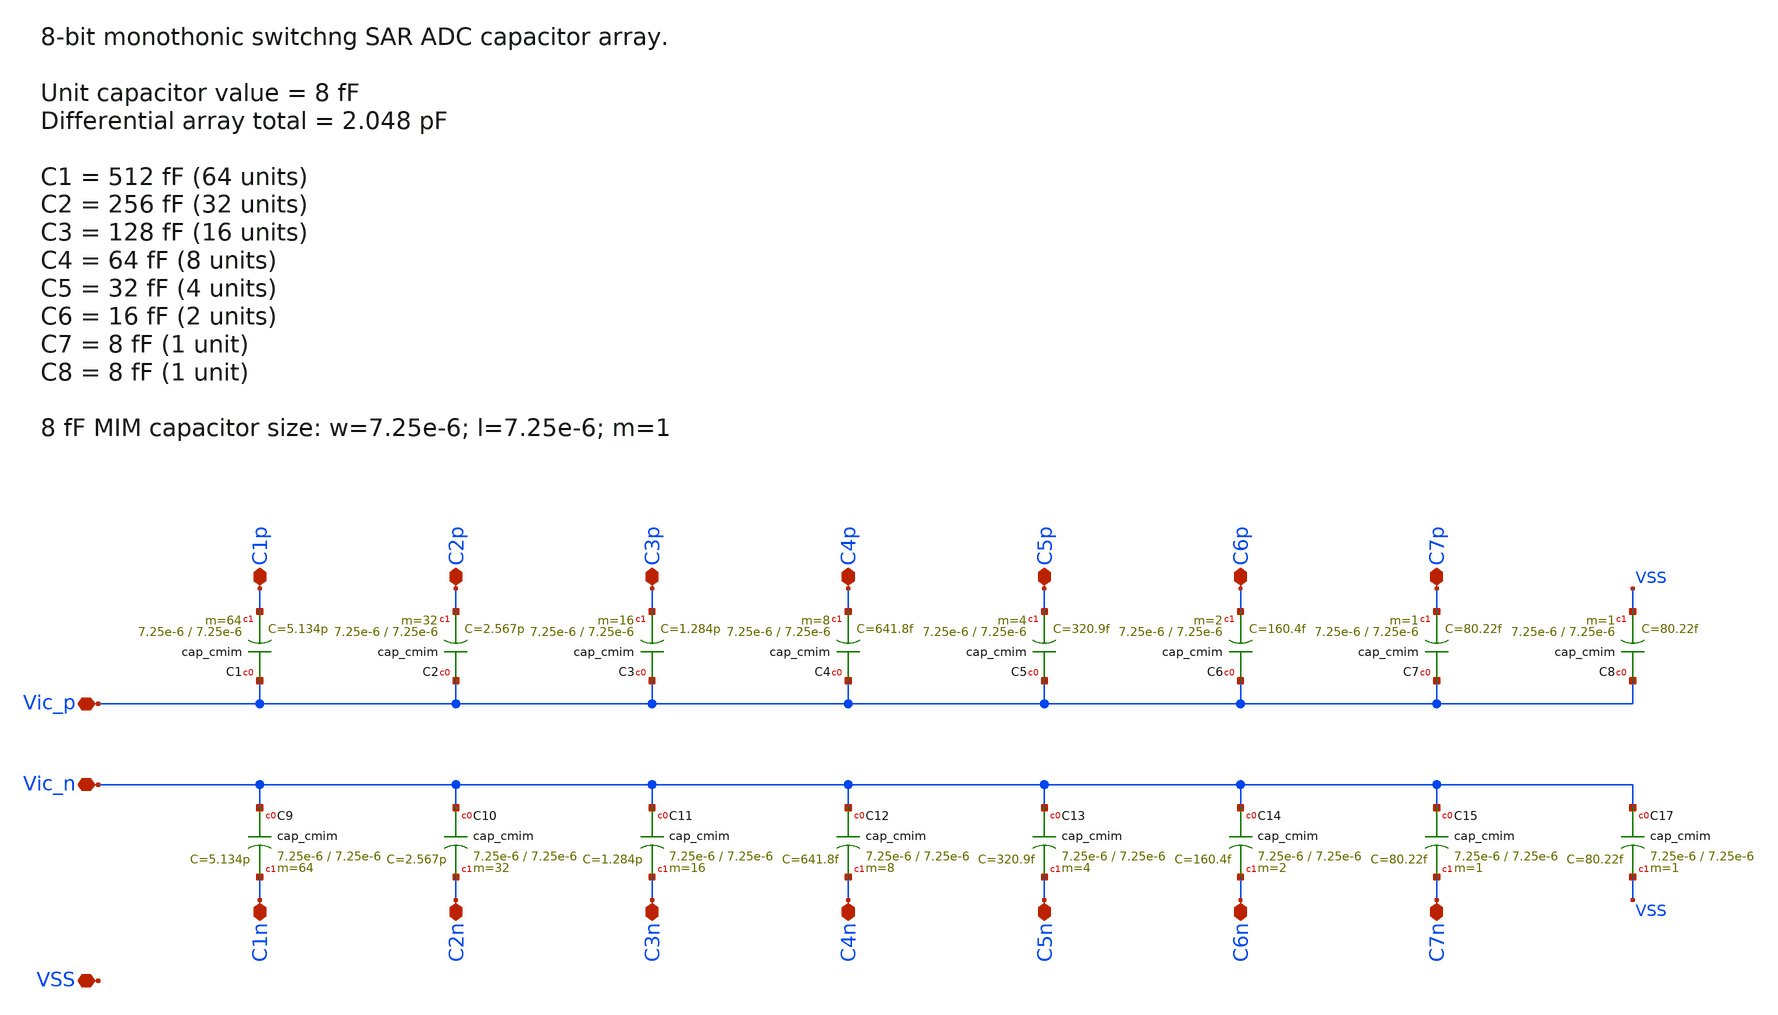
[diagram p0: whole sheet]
** sch_path: sar_adc/xschem/blocks/capacitor_array/capacitor_array.sch
**.subckt capacitor_array Vic_p Vic_n C1p C2p C3p C4p C5p C6p C7p C1n C2n C3n C4n C5n C6n C7n VSS
*.iopin Vic_p
*.iopin Vic_n
*.iopin C1p
*.iopin C2p
*.iopin C3p
*.iopin C4p
*.iopin C5p
*.iopin C6p
*.iopin C7p
*.iopin C1n
*.iopin C2n
*.iopin C3n
*.iopin C4n
*.iopin C5n
*.iopin C6n
*.iopin C7n
*.iopin VSS
XC15 Vic_n C7n cap_cmim w=7.25e-6 l=7.25e-6 m=1 mm_ok=1
XC7 Vic_p C7p cap_cmim w=7.25e-6 l=7.25e-6 m=1 mm_ok=1
XC8 Vic_p VSS cap_cmim w=7.25e-6 l=7.25e-6 m=1 mm_ok=1
XC17 Vic_n VSS cap_cmim w=7.25e-6 l=7.25e-6 m=1 mm_ok=1
XC1 Vic_p C1p cap_cmim w=7.25e-6 l=7.25e-6 m=64 mm_ok=1
XC2 Vic_p C2p cap_cmim w=7.25e-6 l=7.25e-6 m=32 mm_ok=1
XC3 Vic_p C3p cap_cmim w=7.25e-6 l=7.25e-6 m=16 mm_ok=1
XC4 Vic_p C4p cap_cmim w=7.25e-6 l=7.25e-6 m=8 mm_ok=1
XC5 Vic_p C5p cap_cmim w=7.25e-6 l=7.25e-6 m=4 mm_ok=1
XC6 Vic_p C6p cap_cmim w=7.25e-6 l=7.25e-6 m=2 mm_ok=1
XC9 Vic_n C1n cap_cmim w=7.25e-6 l=7.25e-6 m=64 mm_ok=1
XC10 Vic_n C2n cap_cmim w=7.25e-6 l=7.25e-6 m=32 mm_ok=1
XC11 Vic_n C3n cap_cmim w=7.25e-6 l=7.25e-6 m=16 mm_ok=1
XC12 Vic_n C4n cap_cmim w=7.25e-6 l=7.25e-6 m=8 mm_ok=1
XC13 Vic_n C5n cap_cmim w=7.25e-6 l=7.25e-6 m=4 mm_ok=1
XC14 Vic_n C6n cap_cmim w=7.25e-6 l=7.25e-6 m=2 mm_ok=1
**.ends
.end
